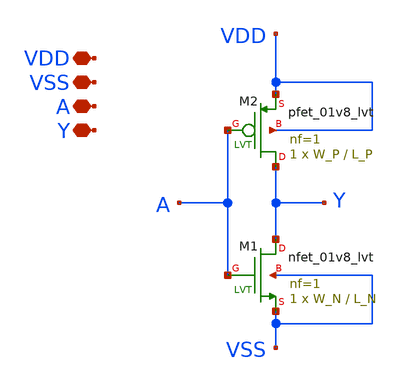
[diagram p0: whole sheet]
** sch_path: inverter/inverter.sch
**.subckt inverter VDD VSS A Y
*.iopin VDD
*.iopin VSS
*.iopin A
*.iopin Y
XM2 Y A VDD VDD sky130_fd_pr__pfet_01v8_lvt L=L_P W=W_P nf=1 ad='int((1 + 1)/2) * W_P / 1 * 0.29' as='int((1 + 2)/2) * W_P / 1 * 0.29'
+ pd='2*int((1 + 1)/2) * (W_P / 1 + 0.29)' ps='2*int((1 + 2)/2) * (W_P / 1 + 0.29)' nrd='0.29 / W_P ' nrs='0.29 / W_P '
+ sa=0 sb=0 sd=0 mult=1 m=1
XM1 Y A VSS VSS sky130_fd_pr__nfet_01v8_lvt L=L_N W=W_N nf=1 ad='int((1 + 1)/2) * W_N / 1 * 0.29' as='int((1 + 2)/2) * W_N / 1 * 0.29'
+ pd='2*int((1 + 1)/2) * (W_N / 1 + 0.29)' ps='2*int((1 + 2)/2) * (W_N / 1 + 0.29)' nrd='0.29 / W_N ' nrs='0.29 / W_N '
+ sa=0 sb=0 sd=0 mult=1 m=1
**.ends
.end
